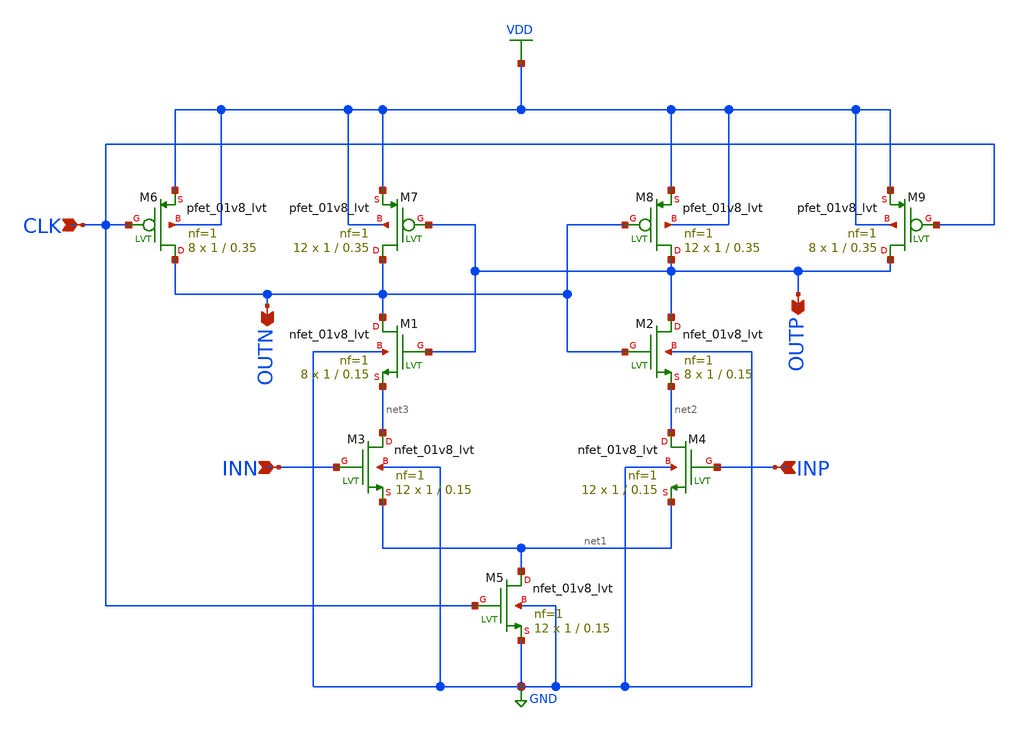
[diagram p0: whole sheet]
** sch_path: my_dynamic_comp.sch
**.subckt my_dynamic_comp INN INP OUTP OUTN CLK
*.ipin INN
*.ipin INP
*.opin OUTP
*.opin OUTN
*.ipin CLK
XM6 OUTN CLK VDD VDD sky130_fd_pr__pfet_01v8_lvt L=0.35 W=1 nf=1 ad='int((nf+1)/2) * W/nf * 0.29' as='int((nf+2)/2) * W/nf * 0.29'
+ pd='2*int((nf+1)/2) * (W/nf + 0.29)' ps='2*int((nf+2)/2) * (W/nf + 0.29)' nrd='0.29 / W' nrs='0.29 / W'
+ sa=0 sb=0 sd=0 mult=8 m=8
XM7 OUTN OUTP VDD VDD sky130_fd_pr__pfet_01v8_lvt L=0.35 W=1 nf=1 ad='int((nf+1)/2) * W/nf * 0.29' as='int((nf+2)/2) * W/nf * 0.29'
+ pd='2*int((nf+1)/2) * (W/nf + 0.29)' ps='2*int((nf+2)/2) * (W/nf + 0.29)' nrd='0.29 / W' nrs='0.29 / W'
+ sa=0 sb=0 sd=0 mult=12 m=12
XM8 OUTP OUTN VDD VDD sky130_fd_pr__pfet_01v8_lvt L=0.35 W=1 nf=1 ad='int((nf+1)/2) * W/nf * 0.29' as='int((nf+2)/2) * W/nf * 0.29'
+ pd='2*int((nf+1)/2) * (W/nf + 0.29)' ps='2*int((nf+2)/2) * (W/nf + 0.29)' nrd='0.29 / W' nrs='0.29 / W'
+ sa=0 sb=0 sd=0 mult=12 m=12
XM9 OUTP CLK VDD VDD sky130_fd_pr__pfet_01v8_lvt L=0.35 W=1 nf=1 ad='int((nf+1)/2) * W/nf * 0.29' as='int((nf+2)/2) * W/nf * 0.29'
+ pd='2*int((nf+1)/2) * (W/nf + 0.29)' ps='2*int((nf+2)/2) * (W/nf + 0.29)' nrd='0.29 / W' nrs='0.29 / W'
+ sa=0 sb=0 sd=0 mult=8 m=8
XM1 OUTN OUTP net3 GND sky130_fd_pr__nfet_01v8_lvt L=0.15 W=1 nf=1 ad='int((nf+1)/2) * W/nf * 0.29' as='int((nf+2)/2) * W/nf * 0.29'
+ pd='2*int((nf+1)/2) * (W/nf + 0.29)' ps='2*int((nf+2)/2) * (W/nf + 0.29)' nrd='0.29 / W' nrs='0.29 / W'
+ sa=0 sb=0 sd=0 mult=8 m=8
XM2 OUTP OUTN net2 GND sky130_fd_pr__nfet_01v8_lvt L=0.15 W=1 nf=1 ad='int((nf+1)/2) * W/nf * 0.29' as='int((nf+2)/2) * W/nf * 0.29'
+ pd='2*int((nf+1)/2) * (W/nf + 0.29)' ps='2*int((nf+2)/2) * (W/nf + 0.29)' nrd='0.29 / W' nrs='0.29 / W'
+ sa=0 sb=0 sd=0 mult=8 m=8
XM3 net3 INN net1 GND sky130_fd_pr__nfet_01v8_lvt L=0.15 W=1 nf=1 ad='int((nf+1)/2) * W/nf * 0.29' as='int((nf+2)/2) * W/nf * 0.29'
+ pd='2*int((nf+1)/2) * (W/nf + 0.29)' ps='2*int((nf+2)/2) * (W/nf + 0.29)' nrd='0.29 / W' nrs='0.29 / W'
+ sa=0 sb=0 sd=0 mult=12 m=12
XM4 net2 INP net1 GND sky130_fd_pr__nfet_01v8_lvt L=0.15 W=1 nf=1 ad='int((nf+1)/2) * W/nf * 0.29' as='int((nf+2)/2) * W/nf * 0.29'
+ pd='2*int((nf+1)/2) * (W/nf + 0.29)' ps='2*int((nf+2)/2) * (W/nf + 0.29)' nrd='0.29 / W' nrs='0.29 / W'
+ sa=0 sb=0 sd=0 mult=12 m=12
XM5 net1 CLK GND GND sky130_fd_pr__nfet_01v8_lvt L=0.15 W=1 nf=1 ad='int((nf+1)/2) * W/nf * 0.29' as='int((nf+2)/2) * W/nf * 0.29'
+ pd='2*int((nf+1)/2) * (W/nf + 0.29)' ps='2*int((nf+2)/2) * (W/nf + 0.29)' nrd='0.29 / W' nrs='0.29 / W'
+ sa=0 sb=0 sd=0 mult=12 m=12
**.ends
.GLOBAL GND
.GLOBAL VDD
.end
